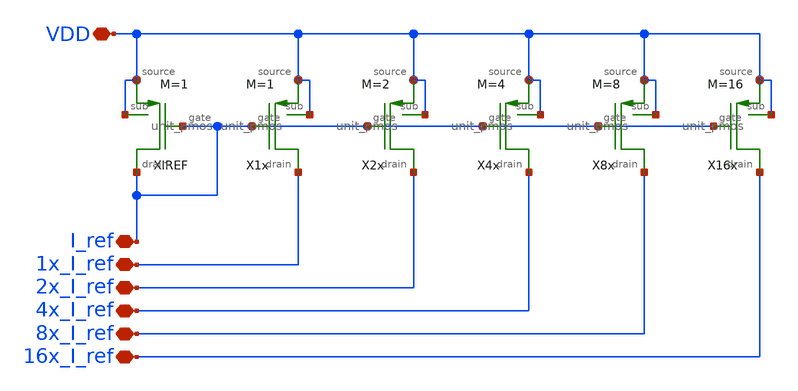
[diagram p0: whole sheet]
** sch_path: designs/libs/core_current_mirror/pmos_current_mirror/pmos_current_mirror.sch
**.subckt pmos_current_mirror I_ref VDD 1x_I_ref 2x_I_ref 4x_I_ref 8x_I_ref 16x_I_ref
*.iopin I_ref
*.iopin VDD
*.iopin 1x_I_ref
*.iopin 2x_I_ref
*.iopin 4x_I_ref
*.iopin 8x_I_ref
*.iopin 16x_I_ref
XIREF I_ref VDD I_ref VDD unit_pmos M=1
X1x 1x_I_ref VDD I_ref VDD unit_pmos M=1
X2x 2x_I_ref VDD I_ref VDD unit_pmos M=2
X4x 4x_I_ref VDD I_ref VDD unit_pmos M=4
X8x 8x_I_ref VDD I_ref VDD unit_pmos M=8
X16x 16x_I_ref VDD I_ref VDD unit_pmos M=16
**.ends

* expanding   symbol:  libs/core_single_mos/unit_pmos/unit_pmos.sym # of pins=4
** sym_path: designs/libs/core_single_mos/unit_pmos/unit_pmos.sym
** sch_path: designs/libs/core_single_mos/unit_pmos/unit_pmos.sch
.subckt unit_pmos drain sub gate source
*.iopin drain
*.iopin source
*.iopin sub
*.iopin gate
**** begin user architecture code

.param M=1

**** end user architecture code
XM1 drain gate source sub pfet_03v3 L=0.5u W=48u nf=8 ad='int((nf+1)/2) * W/nf * 0.18u' as='int((nf+2)/2) * W/nf * 0.18u'
+ pd='2*int((nf+1)/2) * (W/nf + 0.18u)' ps='2*int((nf+2)/2) * (W/nf + 0.18u)' nrd='0.18u / W' nrs='0.18u / W'
+ sa=0 sb=0 sd=0 m={M}
.ends

.end
